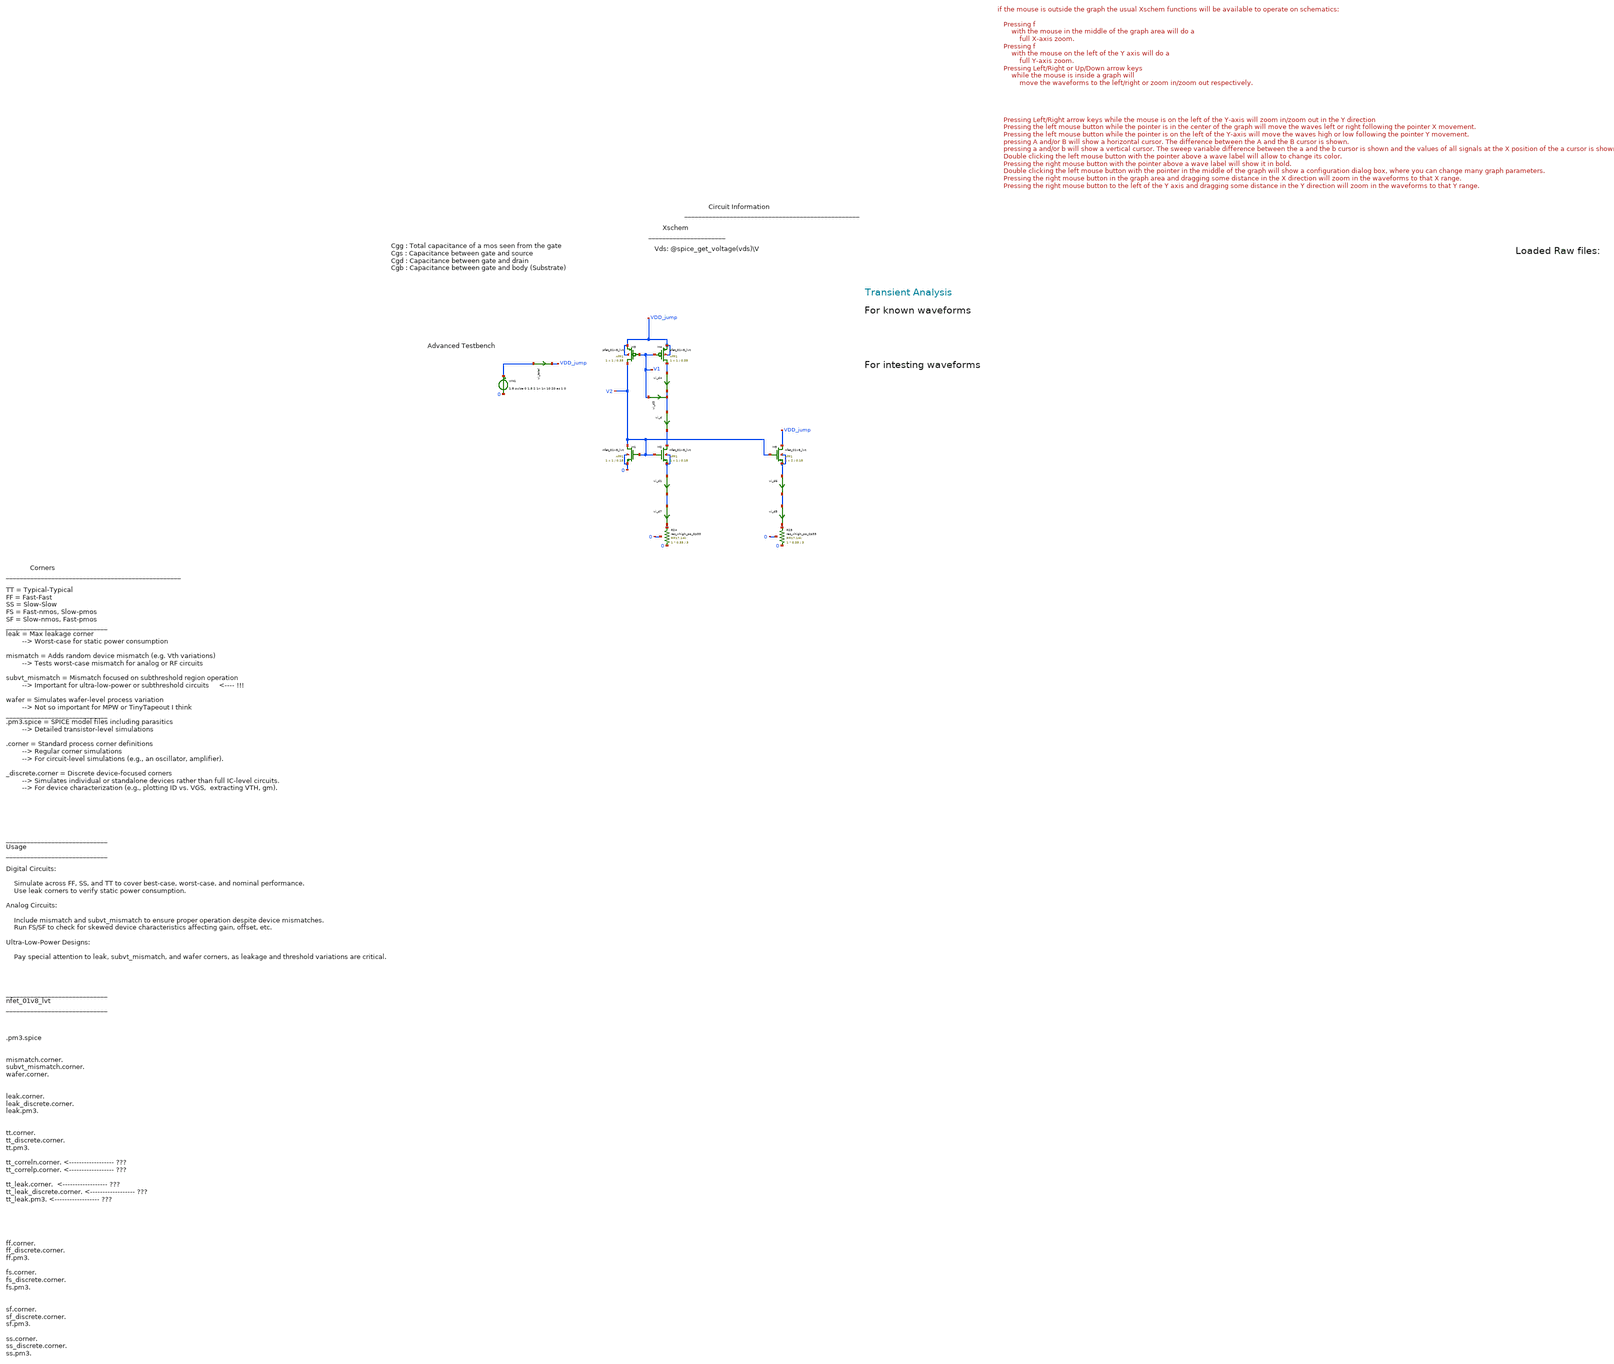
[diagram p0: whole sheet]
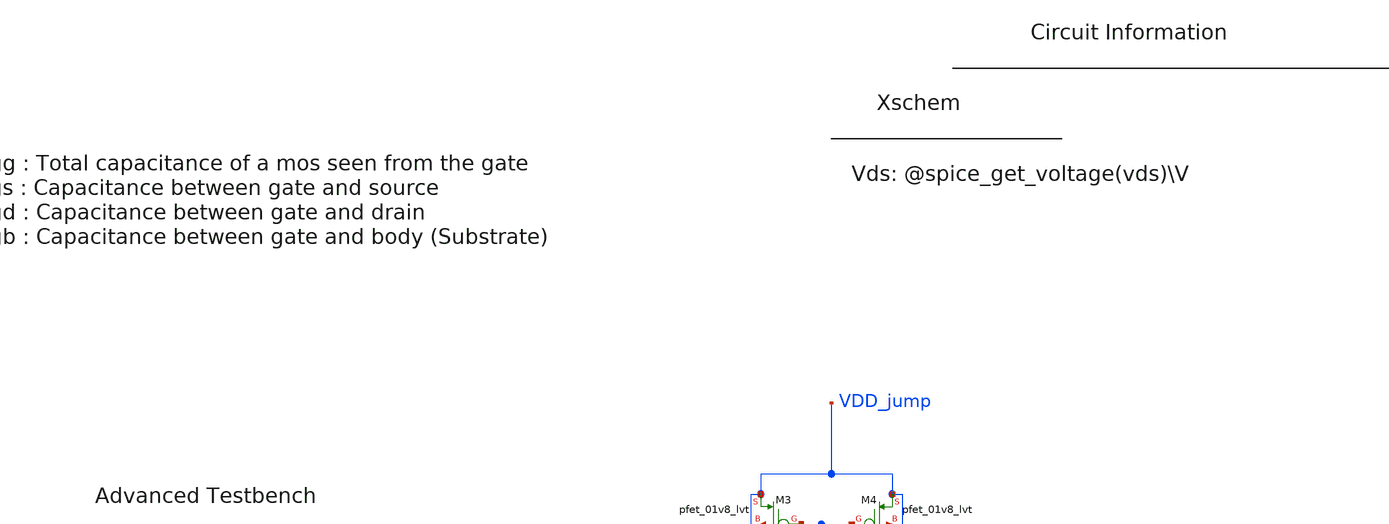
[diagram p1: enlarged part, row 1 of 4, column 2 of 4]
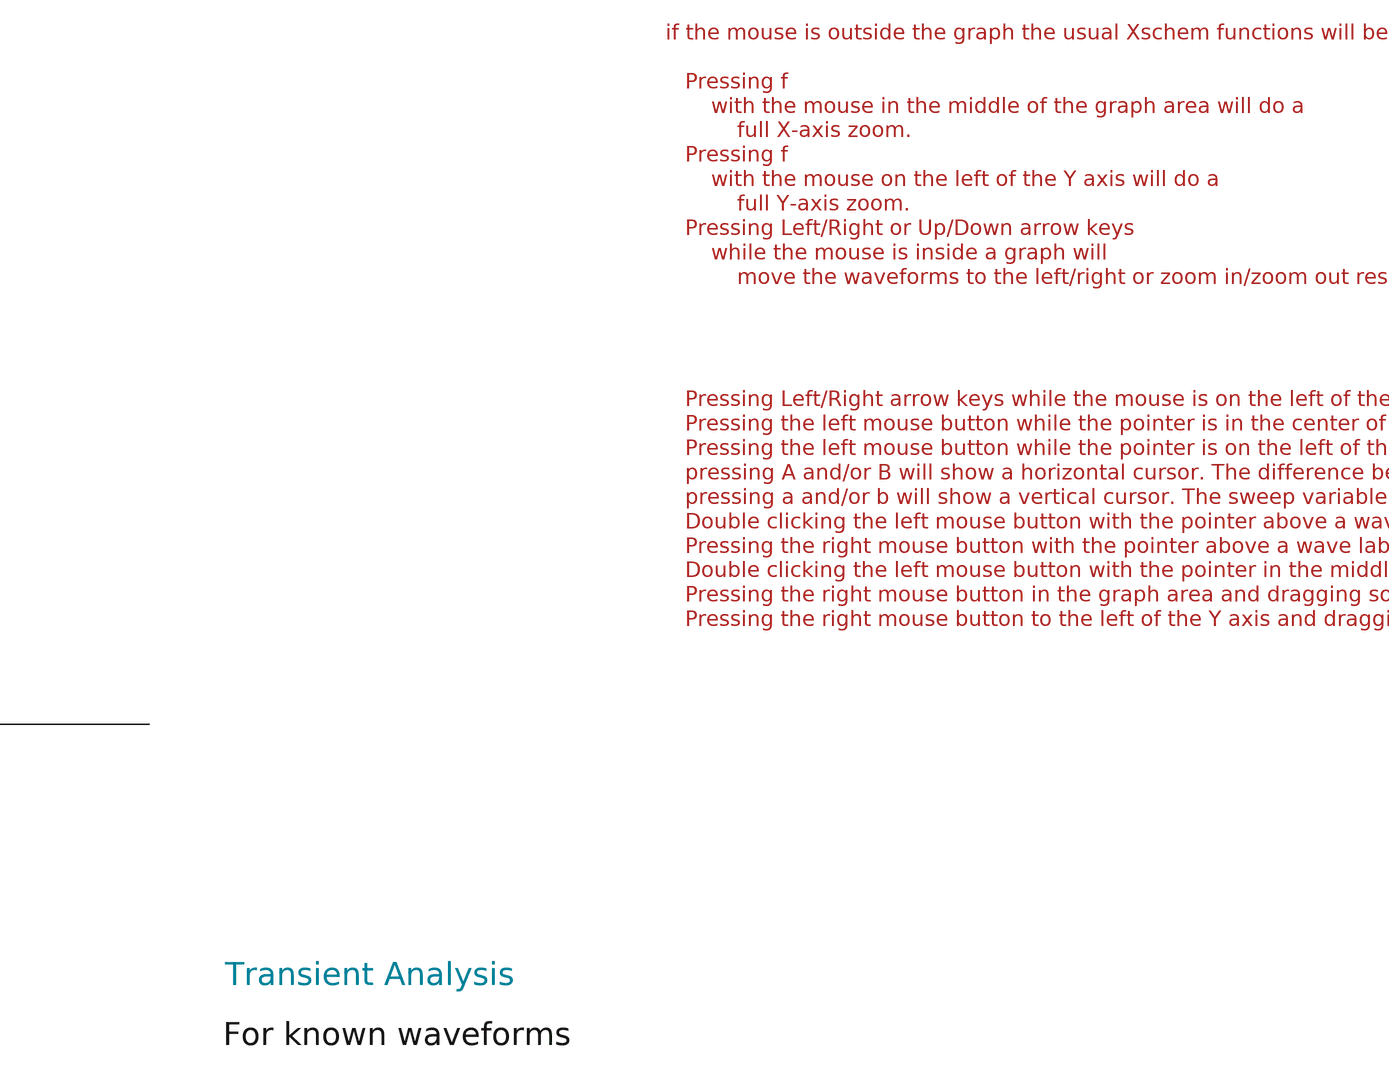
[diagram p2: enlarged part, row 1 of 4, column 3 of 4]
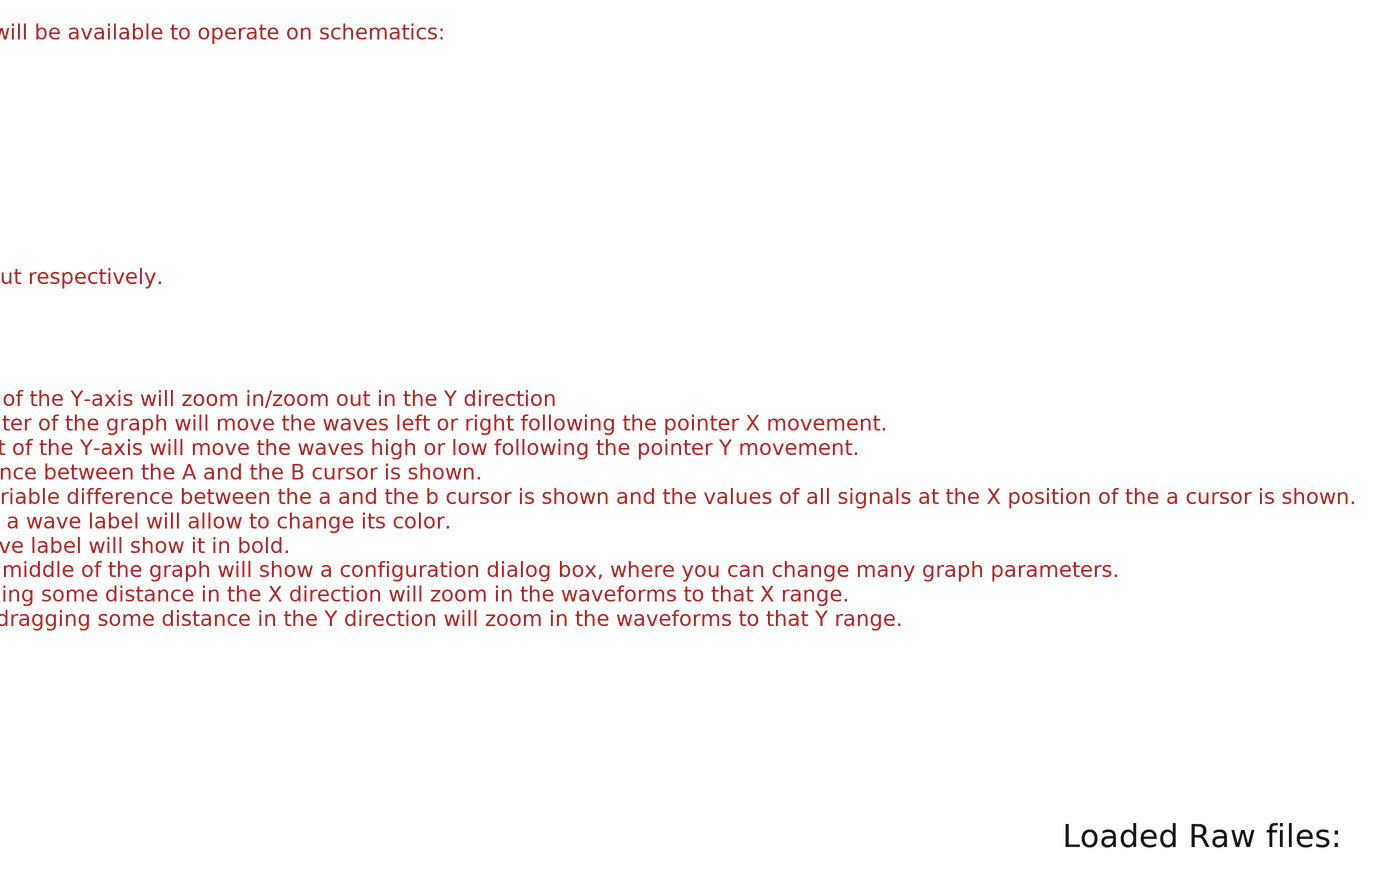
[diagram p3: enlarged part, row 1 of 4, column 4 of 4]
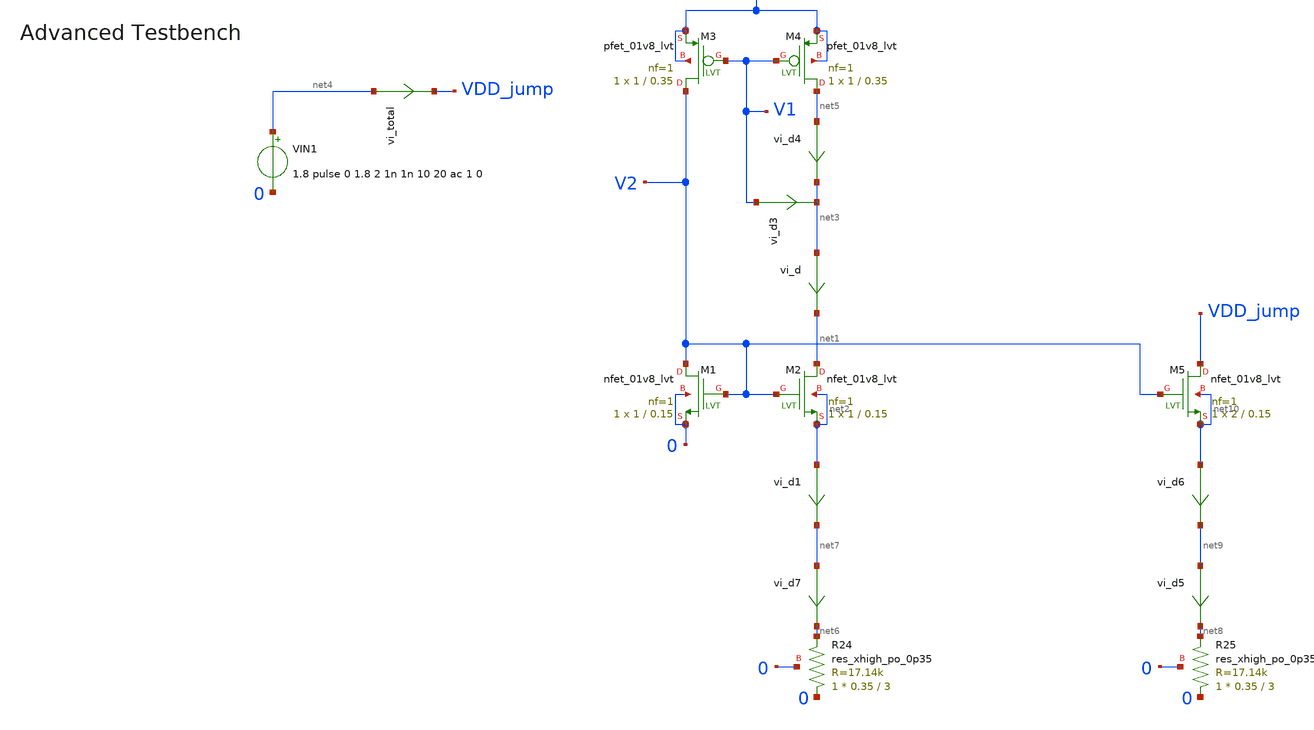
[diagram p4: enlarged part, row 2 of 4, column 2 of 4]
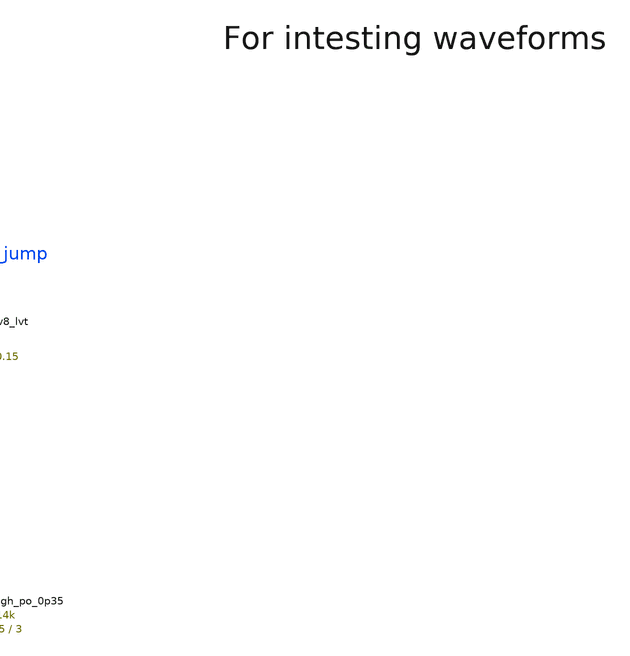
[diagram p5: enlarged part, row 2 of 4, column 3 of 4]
** sch_path: tt10-hdl/tt_um_test_commit/xschem/T2/biasGen/Z_old/basic_currSrc_tb.sch
* Copyright (C) 1998-2024 Stefan Frederik Schippers
* This program is free software; you can redistribute it and/or modify
* it under the terms of the GNU General Public License as published by
* the Free Software Foundation; either version 2 of the License, or
* (at your option) any later version.
* This program is distributed in the hope that it will be useful,
* but WITHOUT ANY WARRANTY; without even the implied warranty of
* MERCHANTABILITY or FITNESS FOR A PARTICULAR PURPOSE.  See the
* GNU General Public License for more details.
* You should have received a copy of the GNU General Public License
* along with this program; if not, write to the Free Software
**.subckt basic_currSrc_tb
vi_d net3 net1 0
.save i(vi_d)
XM1 V2 V2 0 0 sky130_fd_pr__nfet_01v8_lvt L=0.15 W=1 nf=1 ad='int((1 + 1)/2) * 1 / 1 * 0.29' as='int((1 + 2)/2) * 1 / 1 * 0.29'
+ pd='2*int((1 + 1)/2) * (1 / 1 + 0.29)' ps='2*int((1 + 2)/2) * (1 / 1 + 0.29)' nrd='0.29 / 1 ' nrs='0.29 / 1 '
+ sa=0 sb=0 sd=0 mult=1 m=1
XM2 net1 V2 net2 net2 sky130_fd_pr__nfet_01v8_lvt L=0.15 W=1 nf=1 ad='int((1 + 1)/2) * 1 / 1 * 0.29'
+ as='int((1 + 2)/2) * 1 / 1 * 0.29' pd='2*int((1 + 1)/2) * (1 / 1 + 0.29)' ps='2*int((1 + 2)/2) * (1 / 1 + 0.29)'
+ nrd='0.29 / 1 ' nrs='0.29 / 1 ' sa=0 sb=0 sd=0 mult=1 m=1
XM3 V2 V1 VDD_jump VDD_jump sky130_fd_pr__pfet_01v8_lvt L=0.35 W=1 nf=1 ad='int((1 + 1)/2) * 1 / 1 * 0.29'
+ as='int((1 + 2)/2) * 1 / 1 * 0.29' pd='2*int((1 + 1)/2) * (1 / 1 + 0.29)' ps='2*int((1 + 2)/2) * (1 / 1 + 0.29)'
+ nrd='0.29 / 1 ' nrs='0.29 / 1 ' sa=0 sb=0 sd=0 mult=1 m=1
XM4 net5 V1 VDD_jump VDD_jump sky130_fd_pr__pfet_01v8_lvt L=0.35 W=1 nf=1 ad='int((1 + 1)/2) * 1 / 1 * 0.29'
+ as='int((1 + 2)/2) * 1 / 1 * 0.29' pd='2*int((1 + 1)/2) * (1 / 1 + 0.29)' ps='2*int((1 + 2)/2) * (1 / 1 + 0.29)'
+ nrd='0.29 / 1 ' nrs='0.29 / 1 ' sa=0 sb=0 sd=0 mult=1 m=1
VIN1 net4 0 1.8 pulse 0 1.8 2 1n 1n 10 20 ac 1 0
vi_d3 V1 net3 0
.save i(vi_d3)
vi_d4 net5 net3 0
.save i(vi_d4)
vi_d7 net7 net6 0
.save i(vi_d7)
XR24 0 net6 0 sky130_fd_pr__res_xhigh_po_0p35 L=3 mult=1 m=1
vi_d1 net2 net7 0
.save i(vi_d1)
XM5 VDD_jump V2 net10 net10 sky130_fd_pr__nfet_01v8_lvt L=0.15 W=2 nf=1 ad='int((1 + 1)/2) * 2 / 1 * 0.29'
+ as='int((1 + 2)/2) * 2 / 1 * 0.29' pd='2*int((1 + 1)/2) * (2 / 1 + 0.29)' ps='2*int((1 + 2)/2) * (2 / 1 + 0.29)'
+ nrd='0.29 / 2 ' nrs='0.29 / 2 ' sa=0 sb=0 sd=0 mult=1 m=1
vi_d5 net9 net8 0
.save i(vi_d5)
XR25 0 net8 0 sky130_fd_pr__res_xhigh_po_0p35 L=3 mult=1 m=1
vi_d6 net10 net9 0
.save i(vi_d6)
vi_total net4 VDD_jump 0
.save i(vi_total)
**** begin user architecture code



.temp 30

*.option gmin=5n
*.option scale=1e-6
.option wnflag=1
.option savecurrents

.save all
.control
  save all alli

  save @m.xm1.msky130_fd_pr__nfet_01v8_lvt[gm]
  save @m.xm1.msky130_fd_pr__nfet_01v8_lvt[id]
  save @m.xm1.msky130_fd_pr__nfet_01v8_lvt[vgs]

  save @m.xm1.msky130_fd_pr__nfet_01v8_lvt[cgg]
  save @m.xm1.msky130_fd_pr__nfet_01v8_lvt[cgs]
  save @m.xm1.msky130_fd_pr__nfet_01v8_lvt[cgdo]
  save @m.xm1.msky130_fd_pr__nfet_01v8_lvt[cgb]

  save @m.xm1.msky130_fd_pr__nfet_01v8_lvt[vds]
  save @m.xm1.msky130_fd_pr__nfet_01v8_lvt[vdsat]
  save @m.xm1.msky130_fd_pr__nfet_01v8_lvt[vth]


  save @m.xm1.msky130_fd_pr__nfet_01v8_lvt[leff]
  save @m.xm1.msky130_fd_pr__nfet_01v8_lvt[weff]
  save @m.xm1.msky130_fd_pr__nfet_01v8_lvt[gds]
  save @m.xm1.msky130_fd_pr__nfet_01v8_lvt[l]
  save @m.xm1.msky130_fd_pr__nfet_01v8_lvt[w]
  save @m.xm1.msky130_fd_pr__nfet_01v8_lvt[gm]
  save @m.xm1.msky130_fd_pr__nfet_01v8_lvt[gm]
  save @m.xm1.msky130_fd_pr__nfet_01v8_lvt[gm]
  save @m.xm1.msky130_fd_pr__nfet_01v8_lvt[gm]
  save @m.xm1.msky130_fd_pr__nfet_01v8_lvt[gm]



  *dc v_dev_vds 0 1.8 0.005 v_dev_vgs 0 1.8 0.2
  *write nmos_tb.raw




  tran 1m 5000m
  write nmos_tb_tran.raw

  op
  set appendwrite
  write nmos_tb_tran.raw






  *quit 0




.endc





** opencircuitdesign pdks install
.lib $::SKYWATER_MODELS/sky130.lib.spice tt
.include $::SKYWATER_STDCELLS/sky130_fd_sc_hd.spice


**** end user architecture code
**.ends
.end
